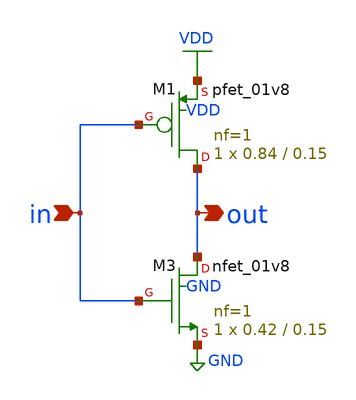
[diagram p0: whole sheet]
** sch_path: Tutorial_5/inverter.sch
**.subckt inverter in out
*.ipin in
*.opin out
XM3 out in GND GND sky130_fd_pr__nfet_01v8 L=0.15 W=0.42 nf=1 ad='int((nf+1)/2) * W/nf * 0.29' as='int((nf+2)/2) * W/nf * 0.29'
+ pd='2*int((nf+1)/2) * (W/nf + 0.29)' ps='2*int((nf+2)/2) * (W/nf + 0.29)' nrd='0.29 / W' nrs='0.29 / W'
+ sa=0 sb=0 sd=0 mult=1 m=1
XM1 out in VDD VDD sky130_fd_pr__pfet_01v8 L=0.15 W=0.84 nf=1 ad='int((nf+1)/2) * W/nf * 0.29' as='int((nf+2)/2) * W/nf * 0.29'
+ pd='2*int((nf+1)/2) * (W/nf + 0.29)' ps='2*int((nf+2)/2) * (W/nf + 0.29)' nrd='0.29 / W' nrs='0.29 / W'
+ sa=0 sb=0 sd=0 mult=1 m=1
**.ends
.GLOBAL GND
.GLOBAL VDD
.end
